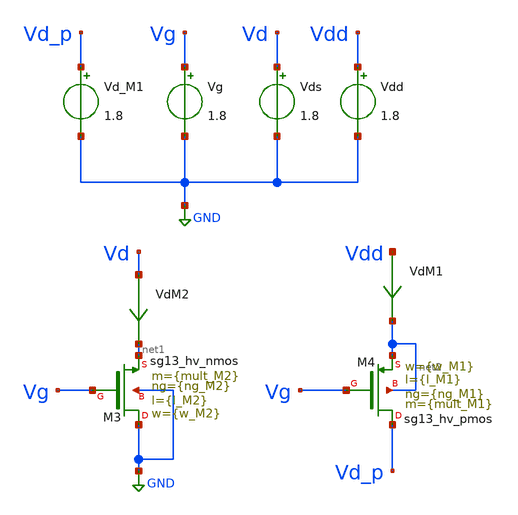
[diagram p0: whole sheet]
** sch_path: xschem/DCDCBuck/TB_MOS_POWER_Sizing.sch
**.subckt TB_MOS_POWER_Sizing
Vg Vg GND 1.8
Vds Vd GND 1.8
Vdd Vdd GND 1.8
VdM1 Vdd net2 0
.save i(vdm1)
VdM2 Vd net1 0
.save i(vdm2)
Vd_M1 Vd_p GND 1.8
XM3 GND Vg net1 GND sg13_hv_nmos w={w_M2} l={l_M2} ng={ng_M2} m={mult_M2} mm_ok=1
XM4 Vd_p Vg net2 net2 sg13_hv_pmos w={w_M1} l={l_M1} ng={ng_M1} m={mult_M1} mm_ok=1
**** begin user architecture code


.save all

.control
reset
alter Vg 1.8
dc Vds 0 0.3 0.01
*dc Vds 0 0.5 0.01 temp 0 27 1
let Vds_M2 = v(Vd)
let Ids_M2 = i(VdM2)

*let G_M2 = Ids_M2/(Vds_M2)
let G_M2 = @m.xm2.msky130_fd_pr__nfet_01v8[gds]
let Ron_M2 = 1/G_M2
let I_M2 = i(VdM2)
let G_M22 = deriv(I_M2)
let Ron_M22 = 1/G_M22

plot Ron_M2 vs Vds_M2
plot Ids_M2 vs Vds_M2

meas dc I_M2 FIND Ids_M2 AT=100m

.endc

.control
reset
alter Vg 0
dc Vd_M1 1.5 1.8 0.01
*dc Vd_M1 2 1.8 0.01 temp 0 27 1

let Vsd_M1 = v(Vdd) -v(Vd_p)
let Isd_M1 = i(VdM1)

let G_M1 = Isd_M1/Vsd_M1
let Ron_M1 = 1/G_M1

plot Isd_M1 vs Vsd_M1
plot Ron_M1 vs Vsd_M1

meas dc I_M1 FIND Isd_M1 AT=1.7

.endc

.end




.param temp=27
.param mult_M1 = 9000
.param w_M1 =10
.param l_M1 = 0.15
.param ng_M1 = 1

.param mult_M2 = 2000
.param w_M2 =10
.param l_M2 =0.15
.param ng_M2 =1





**** end user architecture code
**.ends
.GLOBAL GND
.end
